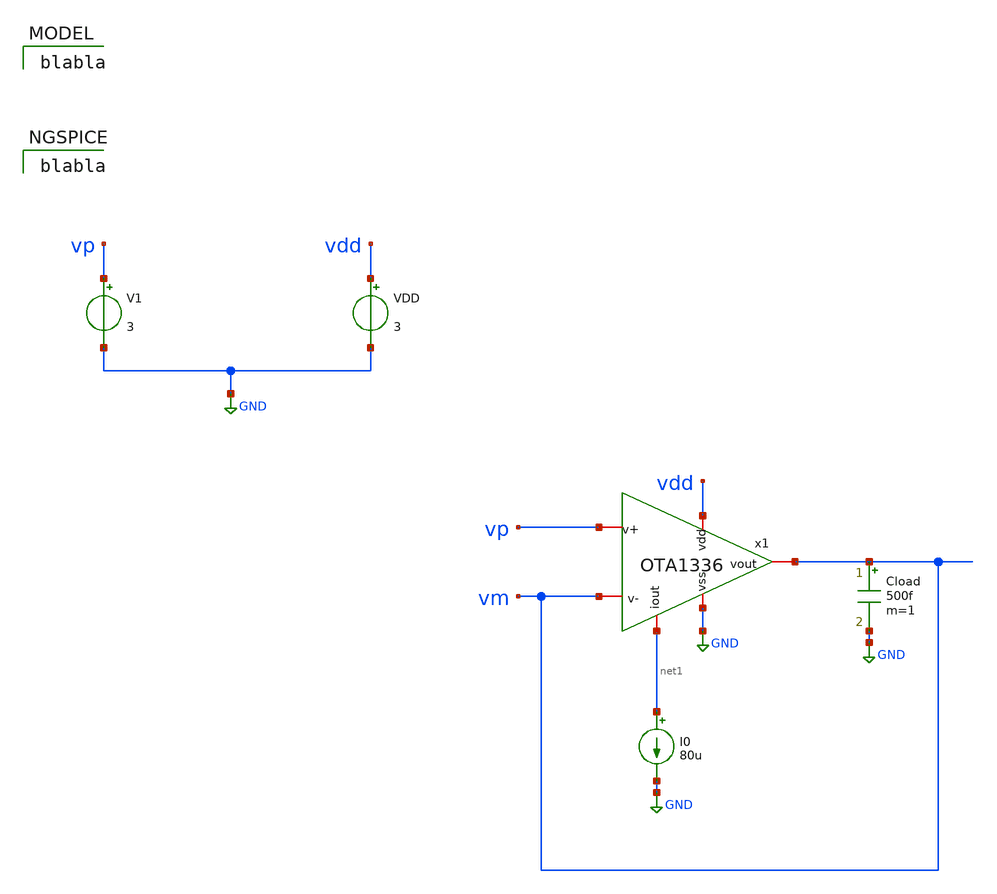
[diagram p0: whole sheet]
** sch_path: tests/data/OTA1336/testbenches/tran/xschem/payload/OTA1336_tb.sch
**.subckt OTA1336_tb
V1 vp GND 3
VDD vdd GND 3
I0 net1 GND 80u
Cload vm GND 500f m=1
x1 vdd net1 vm vm vp GND OTA1336
**** begin user architecture code
 value=

blabla

**** end user architecture code
**.ends
.GLOBAL GND
.end
